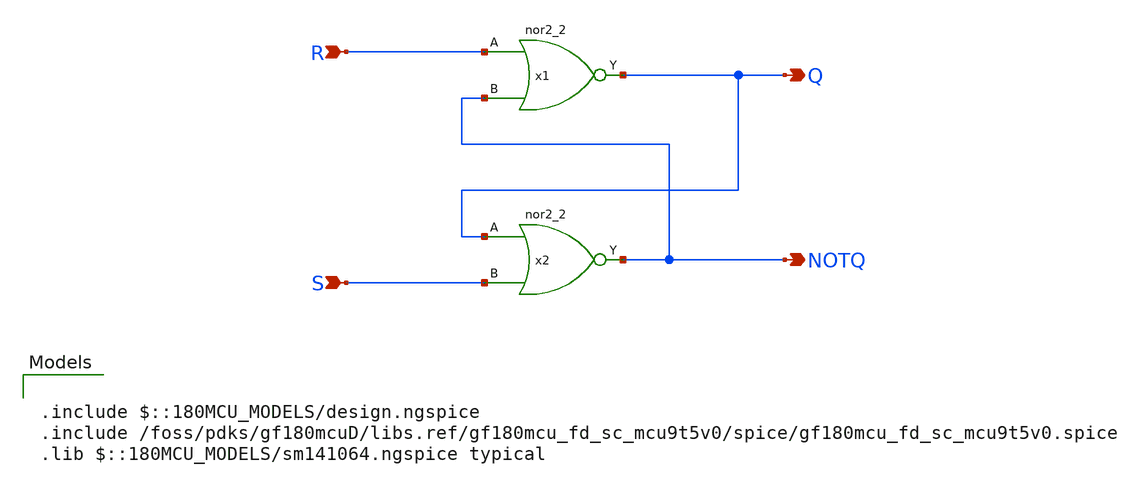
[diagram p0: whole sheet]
** sch_path: designs/libs/core_analog/oscillator/sr_latch.sch
**.subckt sr_latch R S Q NOTQ
*.ipin R
*.ipin S
*.opin Q
*.opin NOTQ
x1 R NOTQ VSSd VDDd VSSd VDDd Q gf180mcu_fd_sc_mcu9t5v0__nor2_2
x2 Q S VSSd VDDd VSSd VDDd NOTQ gf180mcu_fd_sc_mcu9t5v0__nor2_2
**** begin user architecture code

.include $::180MCU_MODELS/design.ngspice
.include /foss/pdks/gf180mcuD/libs.ref/gf180mcu_fd_sc_mcu9t5v0/spice/gf180mcu_fd_sc_mcu9t5v0.spice
.lib $::180MCU_MODELS/sm141064.ngspice typical

**** end user architecture code
**.ends
.end
